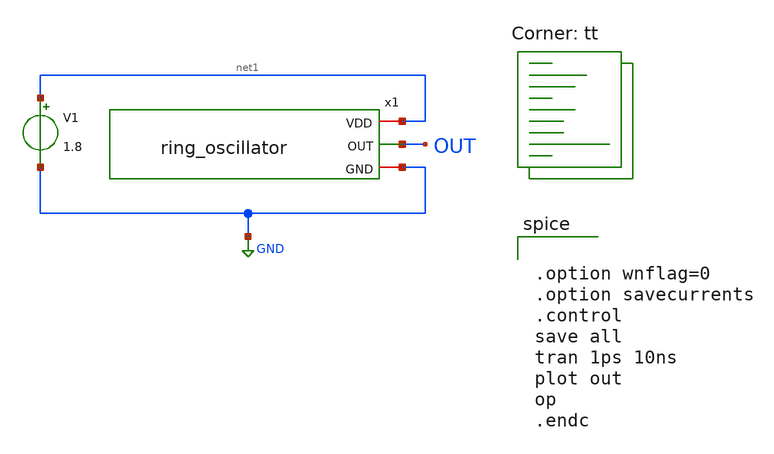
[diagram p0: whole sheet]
** sch_path: ring_oscillator/ring_oscillator_tb.sch
**.subckt ring_oscillator_tb
x1 net1 OUT GND ring_oscillator
V1 net1 GND 1.8
**** begin user architecture code


.option wnflag=0
.option savecurrents
.control
save all
tran 1ps 10ns
plot out
op
.endc


.lib $::SKYWATER_MODELS/sky130.lib.spice tt
**** end user architecture code
**.ends

* expanding   symbol:  ring_oscillator.sym # of pins=3
** sym_path: ring_oscillator/ring_oscillator.sym
** sch_path: ring_oscillator/ring_oscillator.sch
.subckt ring_oscillator VDD OUT GND
*.iopin VDD
*.iopin GND
*.opin OUT
x1 VDD OUT net1 GND inverter
x2 VDD net1 net2 GND inverter
x3 VDD net2 OUT GND inverter
.ends


* expanding   symbol:  inverter.sym # of pins=4
** sym_path: ring_oscillator/inverter.sym
** sch_path: ring_oscillator/inverter.sch
.subckt inverter VDD IN OUT GND
*.ipin IN
*.iopin VDD
*.iopin GND
*.opin OUT
XM1 OUT IN GND GND sky130_fd_pr__nfet_01v8 L=0.15 W=1 nf=1 ad='int((nf+1)/2) * W/nf * 0.29' as='int((nf+2)/2) * W/nf * 0.29'
+ pd='2*int((nf+1)/2) * (W/nf + 0.29)' ps='2*int((nf+2)/2) * (W/nf + 0.29)' nrd='0.29 / W' nrs='0.29 / W'
+ sa=0 sb=0 sd=0 mult=1 m=1
XM2 OUT IN VDD VDD sky130_fd_pr__pfet_01v8 L=0.15 W=1 nf=1 ad='int((nf+1)/2) * W/nf * 0.29' as='int((nf+2)/2) * W/nf * 0.29'
+ pd='2*int((nf+1)/2) * (W/nf + 0.29)' ps='2*int((nf+2)/2) * (W/nf + 0.29)' nrd='0.29 / W' nrs='0.29 / W'
+ sa=0 sb=0 sd=0 mult=1 m=1
.ends

.GLOBAL GND
.end
